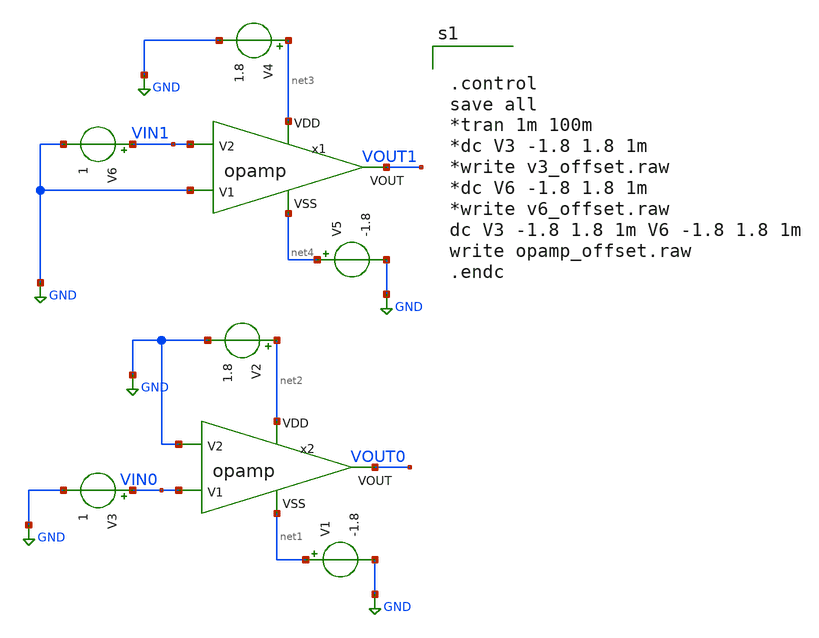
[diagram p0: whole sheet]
** sch_path: opamp_offset.sch
**.subckt opamp_offset
V2 net2 GND 1.8
V1 net1 GND -1.8
V3 VIN0 GND 1
V5 net4 GND -1.8
V6 VIN1 GND 1
V4 net3 GND 1.8
x1 net3 net4 GND VIN1 VOUT1 opamp
x2 net2 net1 VIN0 GND VOUT0 opamp
**** begin user architecture code


.control
save all
*tran 1m 100m
*dc V3 -1.8 1.8 1m
*write v3_offset.raw
*dc V6 -1.8 1.8 1m
*write v6_offset.raw
dc V3 -1.8 1.8 1m V6 -1.8 1.8 1m
write opamp_offset.raw
.endc



** opencircuitdesign pdks install
.lib $::SKYWATER_MODELS/sky130.lib.spice tt


**** end user architecture code
**.ends

* expanding   symbol:  ../xschem/opamp.sym # of pins=5
** sym_path: ../xschem/opamp.sym
** sch_path: ../xschem/opamp.sch
.subckt opamp VDD VSS V1 V2 VOUT
*.ipin VSS
*.ipin VDD
*.ipin V2
*.ipin V1
*.opin VOUT
XM2 net2 V2 net1 VSS sky130_fd_pr__nfet_g5v0d10v5 L=1 W=17.45 nf=1 ad='int((nf+1)/2) * W/nf * 0.29' as='int((nf+2)/2) * W/nf * 0.29'
+ pd='2*int((nf+1)/2) * (W/nf + 0.29)' ps='2*int((nf+2)/2) * (W/nf + 0.29)' nrd='0.29 / W' nrs='0.29 / W'
+ sa=0 sb=0 sd=0 mult=1 m=1
XM1 net3 net2 VDD VDD sky130_fd_pr__pfet_g5v0d10v5 L=1 W=30 nf=1 ad='int((nf+1)/2) * W/nf * 0.29' as='int((nf+2)/2) * W/nf * 0.29'
+ pd='2*int((nf+1)/2) * (W/nf + 0.29)' ps='2*int((nf+2)/2) * (W/nf + 0.29)' nrd='0.29 / W' nrs='0.29 / W'
+ sa=0 sb=0 sd=0 mult=1 m=1
XM4 net3 V1 net1 VSS sky130_fd_pr__nfet_g5v0d10v5 L=1 W=17.45 nf=1 ad='int((nf+1)/2) * W/nf * 0.29' as='int((nf+2)/2) * W/nf * 0.29'
+ pd='2*int((nf+1)/2) * (W/nf + 0.29)' ps='2*int((nf+2)/2) * (W/nf + 0.29)' nrd='0.29 / W' nrs='0.29 / W'
+ sa=0 sb=0 sd=0 mult=1 m=1
XM5 net6 net4 VSS VSS sky130_fd_pr__nfet_g5v0d10v5 L=1 W=15.17 nf=1 ad='int((nf+1)/2) * W/nf * 0.29'
+ as='int((nf+2)/2) * W/nf * 0.29' pd='2*int((nf+1)/2) * (W/nf + 0.29)' ps='2*int((nf+2)/2) * (W/nf + 0.29)'
+ nrd='0.29 / W' nrs='0.29 / W' sa=0 sb=0 sd=0 mult=1 m=1
XM6 net8 net4 VSS VSS sky130_fd_pr__nfet_g5v0d10v5 L=1 W=19 nf=1 ad='int((nf+1)/2) * W/nf * 0.29' as='int((nf+2)/2) * W/nf * 0.29'
+ pd='2*int((nf+1)/2) * (W/nf + 0.29)' ps='2*int((nf+2)/2) * (W/nf + 0.29)' nrd='0.29 / W' nrs='0.29 / W'
+ sa=0 sb=0 sd=0 mult=1 m=1
XM7 net4 net4 VSS VSS sky130_fd_pr__nfet_g5v0d10v5 L=1 W=15.17 nf=1 ad='int((nf+1)/2) * W/nf * 0.29'
+ as='int((nf+2)/2) * W/nf * 0.29' pd='2*int((nf+1)/2) * (W/nf + 0.29)' ps='2*int((nf+2)/2) * (W/nf + 0.29)'
+ nrd='0.29 / W' nrs='0.29 / W' sa=0 sb=0 sd=0 mult=1 m=1
XM3 net2 net2 VDD VDD sky130_fd_pr__pfet_g5v0d10v5 L=1 W=30 nf=1 ad='int((nf+1)/2) * W/nf * 0.29' as='int((nf+2)/2) * W/nf * 0.29'
+ pd='2*int((nf+1)/2) * (W/nf + 0.29)' ps='2*int((nf+2)/2) * (W/nf + 0.29)' nrd='0.29 / W' nrs='0.29 / W'
+ sa=0 sb=0 sd=0 mult=1 m=1
XM8 VOUT net3 VDD VDD sky130_fd_pr__pfet_g5v0d10v5 L=1 W=38 nf=1 ad='int((nf+1)/2) * W/nf * 0.29' as='int((nf+2)/2) * W/nf * 0.29'
+ pd='2*int((nf+1)/2) * (W/nf + 0.29)' ps='2*int((nf+2)/2) * (W/nf + 0.29)' nrd='0.29 / W' nrs='0.29 / W'
+ sa=0 sb=0 sd=0 mult=2 m=2
XC1 net5 net3 sky130_fd_pr__cap_mim_m3_1 W=9 L=9 MF=2 m=2
V_ibias net7 net4 0
.save i(v_ibias)
XR3 net5 VOUT VSS sky130_fd_pr__res_high_po_0p69 L=3.2 mult=1 m=1
V_ibias1 net1 net6 0
.save i(v_ibias1)
I1 net9 net10 63.26u
V_iout VOUT net8 0
.save i(v_iout)
XM9 VDD VDD net7 VSS sky130_fd_pr__nfet_g5v0d10v5 L=1 W=0.69 nf=1 ad='int((nf+1)/2) * W/nf * 0.29' as='int((nf+2)/2) * W/nf * 0.29'
+ pd='2*int((nf+1)/2) * (W/nf + 0.29)' ps='2*int((nf+2)/2) * (W/nf + 0.29)' nrd='0.29 / W' nrs='0.29 / W'
+ sa=0 sb=0 sd=0 mult=1 m=1
.ends

.GLOBAL GND
.end
